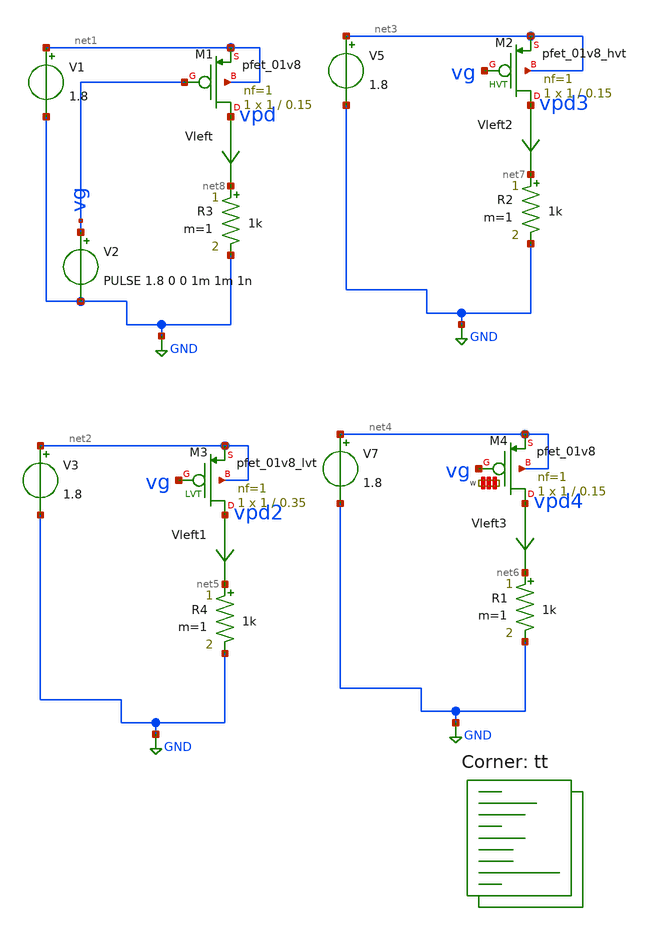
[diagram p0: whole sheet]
** sch_path: Schematics/mos_resistors/pmos_resistor_var.sch
**.subckt pmos_resistor_var
V1 net1 GND 1.8
.save i(v1)
V2 vg GND PULSE 1.8 0 0 1m 1m 1n
.save i(v2)
V3 net2 GND 1.8
.save i(v3)
Vleft1 vpd2 net5 0
.save i(vleft1)
V5 net3 GND 1.8
.save i(v5)
V7 net4 GND 1.8
.save i(v7)
R4 net5 GND 1k m=1
XM1 vpd vg net1 net1 sky130_fd_pr__pfet_01v8 L=0.15 W=1 nf=1 ad='int((nf+1)/2) * W/nf * 0.29' as='int((nf+2)/2) * W/nf * 0.29'
+ pd='2*int((nf+1)/2) * (W/nf + 0.29)' ps='2*int((nf+2)/2) * (W/nf + 0.29)' nrd='0.29 / W' nrs='0.29 / W'
+ sa=0 sb=0 sd=0 mult=1 m=1
XM2 vpd3 vg net3 net3 sky130_fd_pr__pfet_01v8_hvt L=0.15 W=1 nf=1 ad='int((nf+1)/2) * W/nf * 0.29' as='int((nf+2)/2) * W/nf * 0.29'
+ pd='2*int((nf+1)/2) * (W/nf + 0.29)' ps='2*int((nf+2)/2) * (W/nf + 0.29)' nrd='0.29 / W' nrs='0.29 / W'
+ sa=0 sb=0 sd=0 mult=1 m=1
XM3 vpd2 vg net2 net2 sky130_fd_pr__pfet_01v8_lvt L=0.35 W=1 nf=1 ad='int((nf+1)/2) * W/nf * 0.29' as='int((nf+2)/2) * W/nf * 0.29'
+ pd='2*int((nf+1)/2) * (W/nf + 0.29)' ps='2*int((nf+2)/2) * (W/nf + 0.29)' nrd='0.29 / W' nrs='0.29 / W'
+ sa=0 sb=0 sd=0 mult=1 m=1
XM4 vpd4 vg net4 net4 sky130_fd_pr__pfet_01v8 L=0.15 W='1 * 1 ' nf=1 ad='int((nf+1)/2) * W / nf * 0.29'
+ as='int((nf+2)/2) * W / nf * 0.29' pd='2*int((nf+1)/2) * (W / nf + 0.29)' ps='2*int((nf+2)/2) * (W / nf + 0.29)'
+ nrd='0.29 / W ' nrs='0.29 / W ' sa=0 sb=0 sd=0 mult=1 m=1
Vleft3 vpd4 net6 0
.save i(vleft3)
R1 net6 GND 1k m=1
Vleft2 vpd3 net7 0
.save i(vleft2)
R2 net7 GND 1k m=1
Vleft vpd net8 0
.save i(vleft)
R3 net8 GND 1k m=1
**** begin user architecture code
.lib $::SKYWATER_MODELS/sky130.lib.spice tt
**** end user architecture code
**.ends
.GLOBAL GND
**** begin user architecture code

*.options savecurrents
.tran 10u 2m
.save all
.control
	run
	write pmos_resistor_var.raw
.endc


**** end user architecture code
.end
